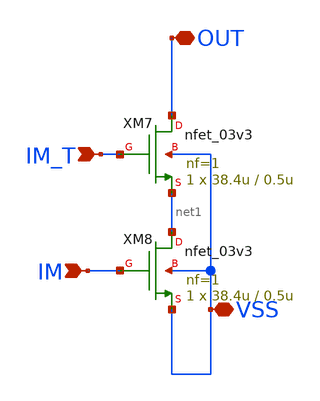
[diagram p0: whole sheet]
** sch_path: DAC_PAKISTAN_01/Pakistan1_Xschem/CM_MSB.sch
**.subckt CM_MSB VSS IM_T IM OUT
*.iopin VSS
*.ipin IM_T
*.ipin IM
*.iopin OUT
XM7 OUT IM_T net1 VSS nfet_03v3 L=0.5u W=38.4u nf=1 ad='int((nf+1)/2) * W/nf * 0.18u' as='int((nf+2)/2) * W/nf * 0.18u'
+ pd='2*int((nf+1)/2) * (W/nf + 0.18u)' ps='2*int((nf+2)/2) * (W/nf + 0.18u)' nrd='0.18u / W' nrs='0.18u / W'
+ sa=0 sb=0 sd=0 m=1
XM8 net1 IM VSS VSS nfet_03v3 L=0.5u W=38.4u nf=1 ad='int((nf+1)/2) * W/nf * 0.18u' as='int((nf+2)/2) * W/nf * 0.18u'
+ pd='2*int((nf+1)/2) * (W/nf + 0.18u)' ps='2*int((nf+2)/2) * (W/nf + 0.18u)' nrd='0.18u / W' nrs='0.18u / W'
+ sa=0 sb=0 sd=0 m=1
**.ends
.end
